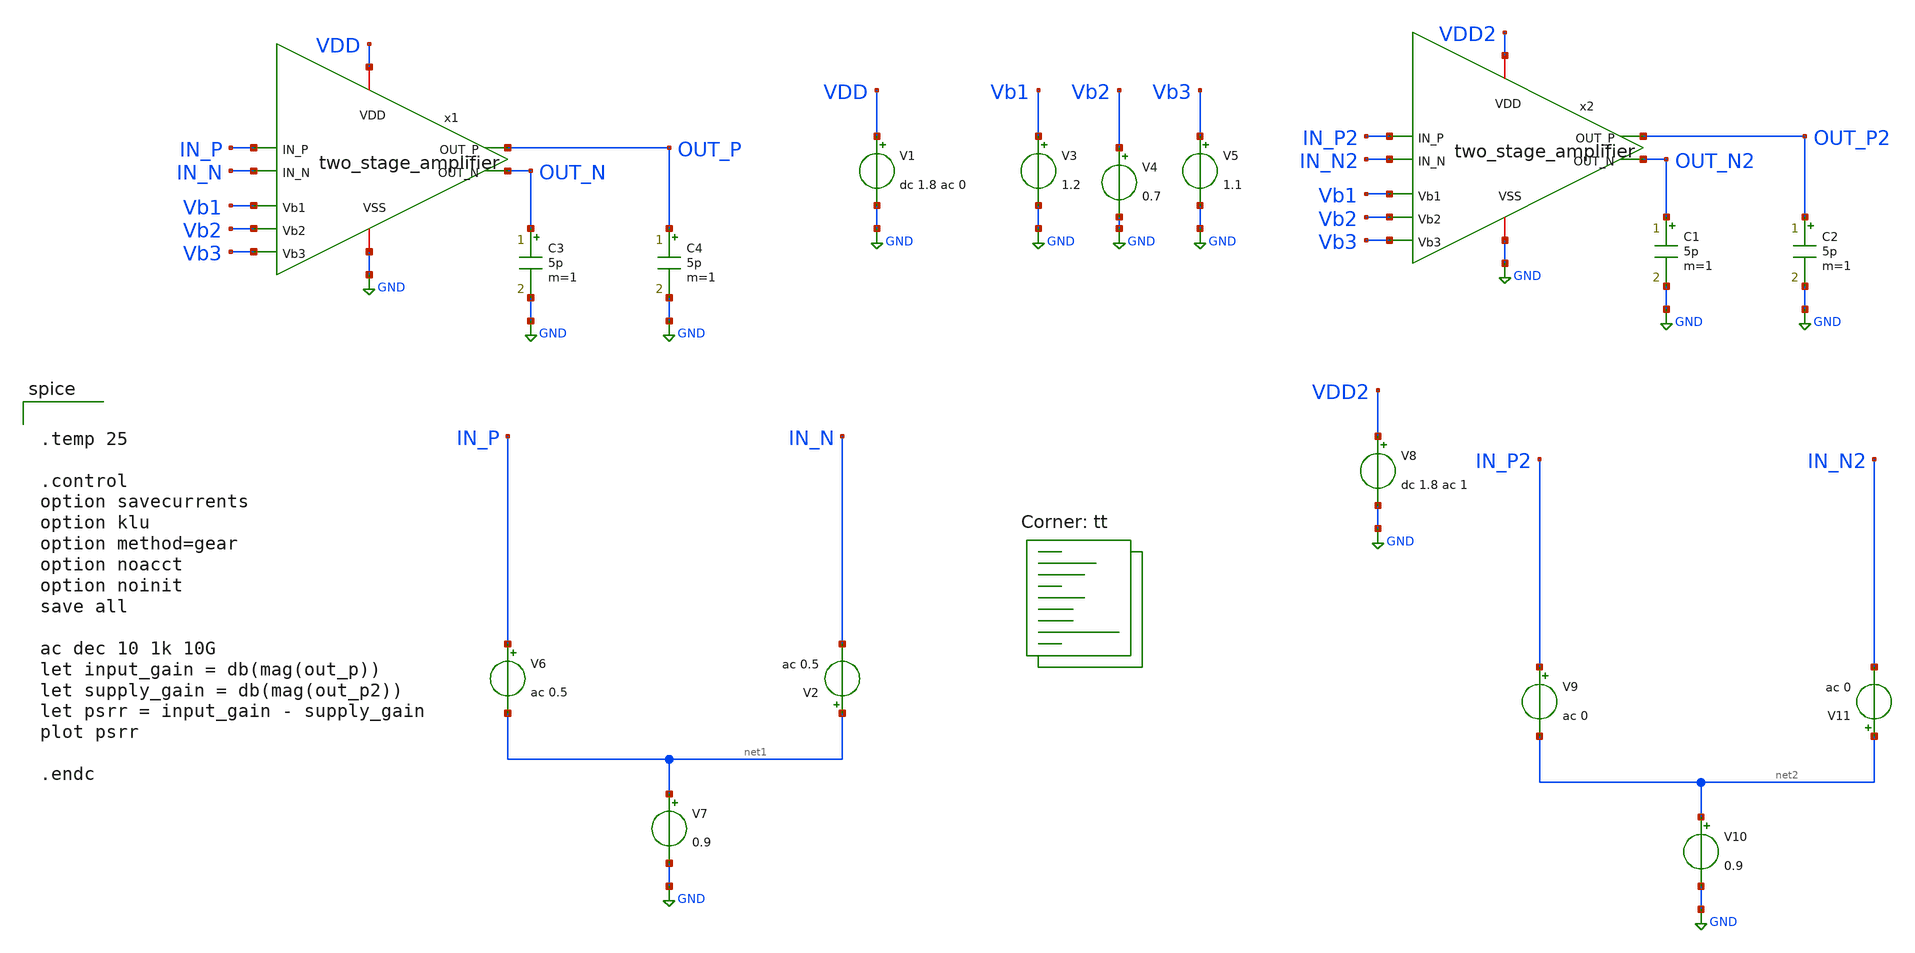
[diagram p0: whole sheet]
** sch_path: xschem/two_stage_amplifier_psrr_tb.sch
**.subckt two_stage_amplifier_psrr_tb
V1 VDD GND dc 1.8 ac 0
.save i(v1)
V3 Vb1 GND 1.2
.save i(v3)
V4 Vb2 GND 0.7
.save i(v4)
V5 Vb3 GND 1.1
.save i(v5)
V6 IN_P net1 ac 0.5
.save i(v6)
x1 VDD Vb3 Vb2 Vb1 IN_P IN_N OUT_P OUT_N GND two_stage_amplifier
C3 OUT_N GND 5p m=1
C4 OUT_P GND 5p m=1
V7 net1 GND 0.9
.save i(v7)
V2 net1 IN_N ac 0.5
.save i(v2)
x2 VDD2 Vb3 Vb2 Vb1 IN_P2 IN_N2 OUT_P2 OUT_N2 GND two_stage_amplifier
C1 OUT_N2 GND 5p m=1
C2 OUT_P2 GND 5p m=1
V8 VDD2 GND dc 1.8 ac 1
.save i(v8)
V9 IN_P2 net2 ac 0
.save i(v9)
V10 net2 GND 0.9
.save i(v10)
V11 net2 IN_N2 ac 0
.save i(v11)
**** begin user architecture code


.temp 25

.control
option savecurrents
option klu
option method=gear
option noacct
option noinit
save all

ac dec 10 1k 10G
let input_gain = db(mag(out_p))
let supply_gain = db(mag(out_p2))
let psrr = input_gain - supply_gain
plot psrr

.endc

.lib $::SKYWATER_MODELS/sky130.lib.spice tt
**** end user architecture code
**.ends

* expanding   symbol:  two_stage_amplifier.sym # of pins=9
** sym_path: xschem/two_stage_amplifier.sym
** sch_path: xschem/two_stage_amplifier.sch
.subckt two_stage_amplifier VDD Vb3 Vb2 Vb1 IN_P IN_N OUT_P OUT_N VSS
*.iopin VSS
*.iopin VDD
*.ipin Vb1
*.ipin Vb2
*.ipin Vb3
*.ipin IN_P
*.ipin IN_N
*.opin OUT_N
*.opin OUT_P
XM1 net1 IN_P net3 VSS sky130_fd_pr__nfet_01v8_lvt L=0.3 W=800 nf=1 ad='int((1 + 1)/2) * 800 / 1 * 0.29'
+ as='int((1 + 2)/2) * 800 / 1 * 0.29' pd='2*int((1 + 1)/2) * (800 / 1 + 0.29)' ps='2*int((1 + 2)/2) * (800 / 1 + 0.29)'
+ nrd='0.29 / 800 ' nrs='0.29 / 800 ' sa=0 sb=0 sd=0 mult=1 m=1
XM2 net2 IN_N net3 VSS sky130_fd_pr__nfet_01v8_lvt L=0.3 W=800 nf=1 ad='int((1 + 1)/2) * 800 / 1 * 0.29'
+ as='int((1 + 2)/2) * 800 / 1 * 0.29' pd='2*int((1 + 1)/2) * (800 / 1 + 0.29)' ps='2*int((1 + 2)/2) * (800 / 1 + 0.29)'
+ nrd='0.29 / 800 ' nrs='0.29 / 800 ' sa=0 sb=0 sd=0 mult=1 m=1
XM3 T_OUT_N Vb1 net1 VSS sky130_fd_pr__nfet_01v8_lvt L=0.3 W=800 nf=1 ad='int((1 + 1)/2) * 800 / 1 * 0.29'
+ as='int((1 + 2)/2) * 800 / 1 * 0.29' pd='2*int((1 + 1)/2) * (800 / 1 + 0.29)' ps='2*int((1 + 2)/2) * (800 / 1 + 0.29)'
+ nrd='0.29 / 800 ' nrs='0.29 / 800 ' sa=0 sb=0 sd=0 mult=1 m=1
XM4 T_OUT_P Vb1 net2 VSS sky130_fd_pr__nfet_01v8_lvt L=0.3 W=800 nf=1 ad='int((1 + 1)/2) * 800 / 1 * 0.29'
+ as='int((1 + 2)/2) * 800 / 1 * 0.29' pd='2*int((1 + 1)/2) * (800 / 1 + 0.29)' ps='2*int((1 + 2)/2) * (800 / 1 + 0.29)'
+ nrd='0.29 / 800 ' nrs='0.29 / 800 ' sa=0 sb=0 sd=0 mult=1 m=1
XM5 T_OUT_N Vb2 net4 net4 sky130_fd_pr__pfet_01v8_lvt L=0.8 W=600 nf=1 ad='int((1 + 1)/2) * 600 / 1 * 0.29'
+ as='int((1 + 2)/2) * 600 / 1 * 0.29' pd='2*int((1 + 1)/2) * (600 / 1 + 0.29)' ps='2*int((1 + 2)/2) * (600 / 1 + 0.29)'
+ nrd='0.29 / 600 ' nrs='0.29 / 600 ' sa=0 sb=0 sd=0 mult=1 m=1
XM6 T_OUT_P Vb2 net5 net5 sky130_fd_pr__pfet_01v8_lvt L=0.8 W=600 nf=1 ad='int((1 + 1)/2) * 600 / 1 * 0.29'
+ as='int((1 + 2)/2) * 600 / 1 * 0.29' pd='2*int((1 + 1)/2) * (600 / 1 + 0.29)' ps='2*int((1 + 2)/2) * (600 / 1 + 0.29)'
+ nrd='0.29 / 600 ' nrs='0.29 / 600 ' sa=0 sb=0 sd=0 mult=1 m=1
XM7 net4 Vb3 VDD VDD sky130_fd_pr__pfet_01v8_lvt L=0.8 W=600 nf=1 ad='int((1 + 1)/2) * 600 / 1 * 0.29'
+ as='int((1 + 2)/2) * 600 / 1 * 0.29' pd='2*int((1 + 1)/2) * (600 / 1 + 0.29)' ps='2*int((1 + 2)/2) * (600 / 1 + 0.29)'
+ nrd='0.29 / 600 ' nrs='0.29 / 600 ' sa=0 sb=0 sd=0 mult=1 m=1
XM8 net5 Vb3 VDD VDD sky130_fd_pr__pfet_01v8_lvt L=0.8 W=600 nf=1 ad='int((1 + 1)/2) * 600 / 1 * 0.29'
+ as='int((1 + 2)/2) * 600 / 1 * 0.29' pd='2*int((1 + 1)/2) * (600 / 1 + 0.29)' ps='2*int((1 + 2)/2) * (600 / 1 + 0.29)'
+ nrd='0.29 / 600 ' nrs='0.29 / 600 ' sa=0 sb=0 sd=0 mult=1 m=1
XM9 net3 T_OUT_N VSS VSS sky130_fd_pr__nfet_01v8_lvt L=0.3 W=25 nf=1 ad='int((1 + 1)/2) * 25 / 1 * 0.29'
+ as='int((1 + 2)/2) * 25 / 1 * 0.29' pd='2*int((1 + 1)/2) * (25 / 1 + 0.29)' ps='2*int((1 + 2)/2) * (25 / 1 + 0.29)'
+ nrd='0.29 / 25 ' nrs='0.29 / 25 ' sa=0 sb=0 sd=0 mult=1 m=1
XM10 net3 T_OUT_P VSS VSS sky130_fd_pr__nfet_01v8_lvt L=0.3 W=25 nf=1 ad='int((1 + 1)/2) * 25 / 1 * 0.29'
+ as='int((1 + 2)/2) * 25 / 1 * 0.29' pd='2*int((1 + 1)/2) * (25 / 1 + 0.29)' ps='2*int((1 + 2)/2) * (25 / 1 + 0.29)'
+ nrd='0.29 / 25 ' nrs='0.29 / 25 ' sa=0 sb=0 sd=0 mult=1 m=1
XM12 OUT_N T_OUT_P VDD VDD sky130_fd_pr__pfet_01v8_lvt L=0.35 W=1000 nf=1 ad='int((1 + 1)/2) * 1000 / 1 * 0.29'
+ as='int((1 + 2)/2) * 1000 / 1 * 0.29' pd='2*int((1 + 1)/2) * (1000 / 1 + 0.29)' ps='2*int((1 + 2)/2) * (1000 / 1 + 0.29)'
+ nrd='0.29 / 1000 ' nrs='0.29 / 1000 ' sa=0 sb=0 sd=0 mult=1 m=1
XM11 OUT_P T_OUT_N VDD VDD sky130_fd_pr__pfet_01v8_lvt L=0.35 W=1000 nf=1 ad='int((1 + 1)/2) * 1000 / 1 * 0.29'
+ as='int((1 + 2)/2) * 1000 / 1 * 0.29' pd='2*int((1 + 1)/2) * (1000 / 1 + 0.29)' ps='2*int((1 + 2)/2) * (1000 / 1 + 0.29)'
+ nrd='0.29 / 1000 ' nrs='0.29 / 1000 ' sa=0 sb=0 sd=0 mult=1 m=1
XM14 OUT_N net6 VSS VSS sky130_fd_pr__nfet_01v8_lvt L=0.35 W=500 nf=1 ad='int((1 + 1)/2) * 500 / 1 * 0.29'
+ as='int((1 + 2)/2) * 500 / 1 * 0.29' pd='2*int((1 + 1)/2) * (500 / 1 + 0.29)' ps='2*int((1 + 2)/2) * (500 / 1 + 0.29)'
+ nrd='0.29 / 500 ' nrs='0.29 / 500 ' sa=0 sb=0 sd=0 mult=1 m=1
XM13 OUT_P net6 VSS VSS sky130_fd_pr__nfet_01v8_lvt L=0.35 W=500 nf=1 ad='int((1 + 1)/2) * 500 / 1 * 0.29'
+ as='int((1 + 2)/2) * 500 / 1 * 0.29' pd='2*int((1 + 1)/2) * (500 / 1 + 0.29)' ps='2*int((1 + 2)/2) * (500 / 1 + 0.29)'
+ nrd='0.29 / 500 ' nrs='0.29 / 500 ' sa=0 sb=0 sd=0 mult=1 m=1
R6 OUT_P net6 1e6 m=1
R7 OUT_N net6 1e6 m=1
XR10 OUT_P net7 sky130_fd_pr__res_generic_po W=1.3 L=1 m=1
XR9 net8 OUT_N sky130_fd_pr__res_generic_po W=1.3 L=1 m=1
XC2 T_OUT_N net7 sky130_fd_pr__cap_mim_m3_1 W=54.6 L=54.6 MF=1 m=1
XC1 T_OUT_P net8 sky130_fd_pr__cap_mim_m3_1 W=54.6 L=54.6 MF=1 m=1
.ends

.GLOBAL GND
.end
